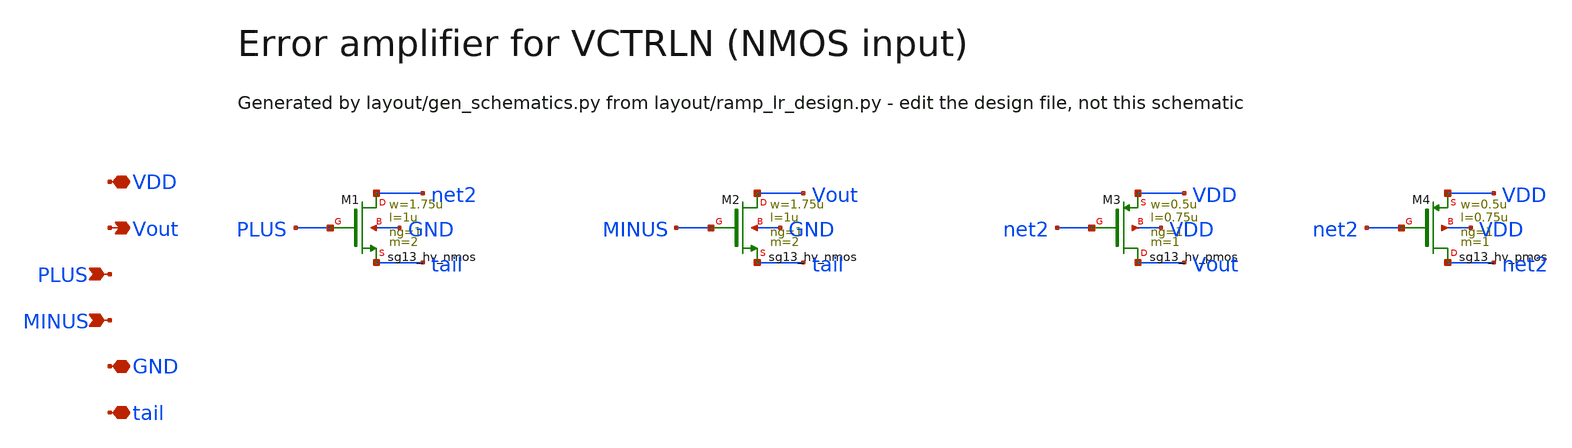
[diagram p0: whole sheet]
** sch_path: Design Files/RAMP/RAMP-LR/NOTA_LR.sch
**.subckt NOTA_LR VDD Vout PLUS MINUS GND tail
*.iopin VDD
*.opin Vout
*.ipin PLUS
*.ipin MINUS
*.iopin GND
*.iopin tail
XM1 net2 PLUS tail GND sg13_hv_nmos w=1.75u l=1u ng=1 m=2 mm_ok=1
XM2 Vout MINUS tail GND sg13_hv_nmos w=1.75u l=1u ng=1 m=2 mm_ok=1
XM3 Vout net2 VDD VDD sg13_hv_pmos w=0.5u l=0.75u ng=1 m=1 mm_ok=1
XM4 net2 net2 VDD VDD sg13_hv_pmos w=0.5u l=0.75u ng=1 m=1 mm_ok=1
**.ends
.end
